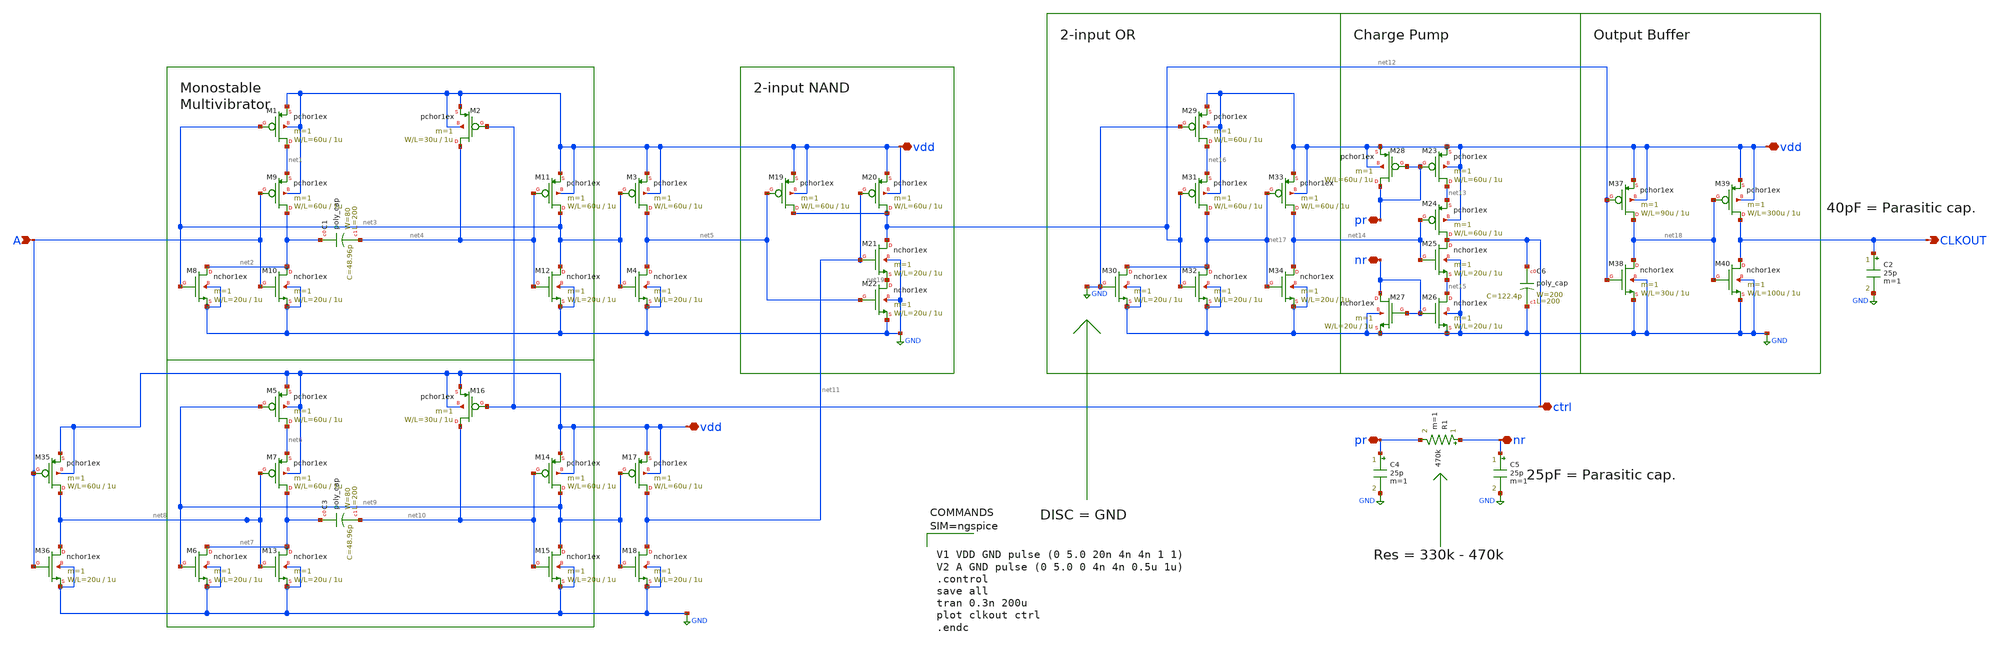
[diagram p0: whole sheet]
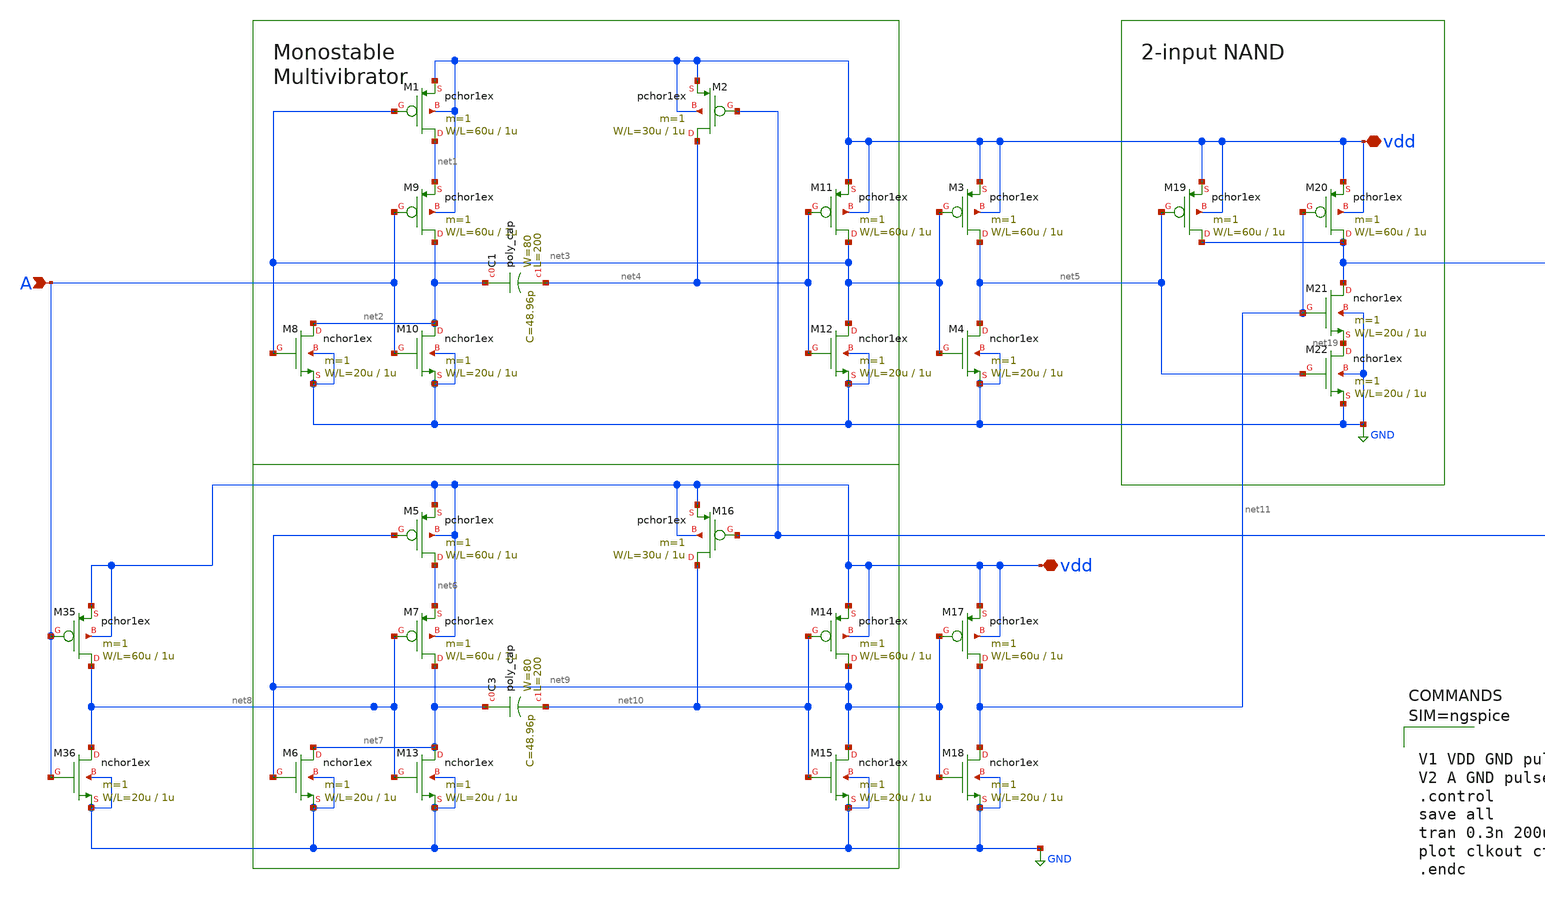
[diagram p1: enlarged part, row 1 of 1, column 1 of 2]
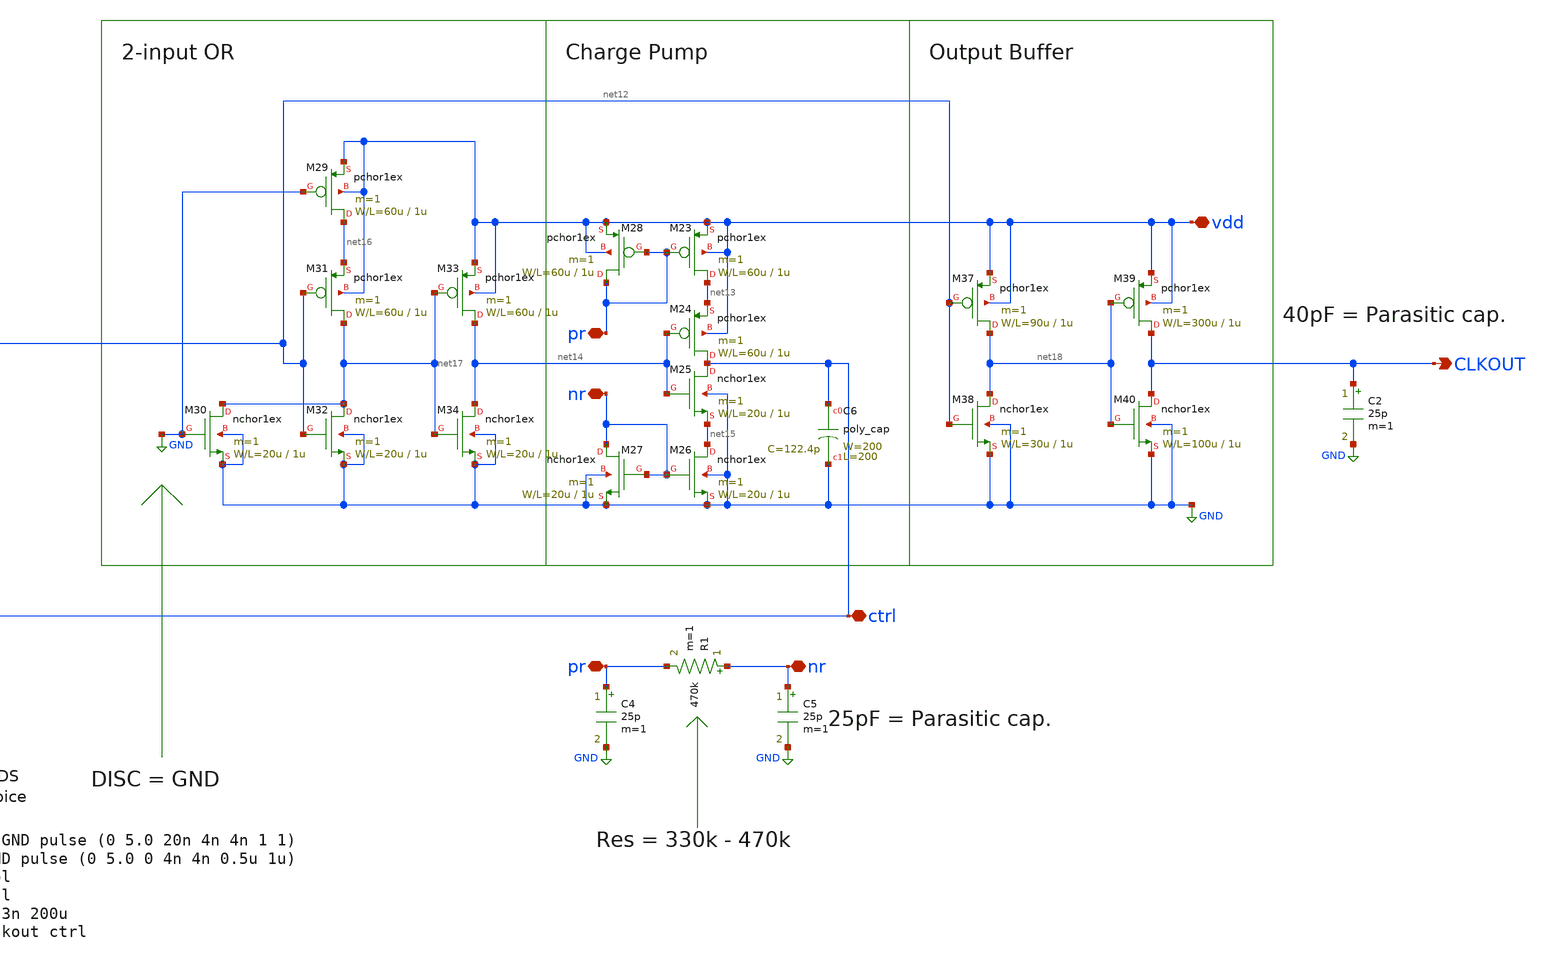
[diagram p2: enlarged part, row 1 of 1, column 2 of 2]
** sch_path: member_project/3zki/clkdb_testbench.sch
**.subckt clkdb_testbench ctrl pr nr CLKOUT vdd A vdd pr nr vdd
*.iopin ctrl
*.iopin pr
*.iopin nr
*.opin CLKOUT
*.iopin vdd
*.ipin A
*.iopin vdd
*.iopin pr
*.iopin nr
*.iopin vdd
C4 pr GND 25p m=1
C5 nr GND 25p m=1
R1 nr pr 470k m=1
C2 CLKOUT GND 25p m=1
M1 net1 net3 vdd vdd pchor1ex L=1u W=60u m=1
M8 net2 net3 GND GND nchor1ex L=1u W=20u m=1
M9 net2 A net1 vdd pchor1ex L=1u W=60u m=1
M10 net2 A GND GND nchor1ex L=1u W=20u m=1
M11 net3 net4 vdd vdd pchor1ex L=1u W=60u m=1
M12 net3 net4 GND GND nchor1ex L=1u W=20u m=1
C1 net2 net4 poly_cap W=80 L=200
M2 net4 ctrl vdd vdd pchor1ex L=1u W=30u m=1
M3 net5 net3 vdd vdd pchor1ex L=1u W=60u m=1
M4 net5 net3 GND GND nchor1ex L=1u W=20u m=1
M5 net6 net9 vdd vdd pchor1ex L=1u W=60u m=1
M6 net7 net9 GND GND nchor1ex L=1u W=20u m=1
M7 net7 net8 net6 vdd pchor1ex L=1u W=60u m=1
M13 net7 net8 GND GND nchor1ex L=1u W=20u m=1
M14 net9 net10 vdd vdd pchor1ex L=1u W=60u m=1
M15 net9 net10 GND GND nchor1ex L=1u W=20u m=1
C3 net7 net10 poly_cap W=80 L=200
M16 net10 ctrl vdd vdd pchor1ex L=1u W=30u m=1
M17 net11 net9 vdd vdd pchor1ex L=1u W=60u m=1
M18 net11 net9 GND GND nchor1ex L=1u W=20u m=1
M35 net8 A vdd vdd pchor1ex L=1u W=60u m=1
M36 net8 A GND GND nchor1ex L=1u W=20u m=1
M19 net12 net5 vdd vdd pchor1ex L=1u W=60u m=1
M20 net12 net11 vdd vdd pchor1ex L=1u W=60u m=1
M21 net12 net11 net19 GND nchor1ex L=1u W=20u m=1
M22 net19 net5 GND GND nchor1ex L=1u W=20u m=1
M23 net13 pr vdd vdd pchor1ex L=1u W=60u m=1
M24 ctrl net14 net13 vdd pchor1ex L=1u W=60u m=1
M25 ctrl net14 net15 GND nchor1ex L=1u W=20u m=1
M26 net15 nr GND GND nchor1ex L=1u W=20u m=1
M27 nr nr GND GND nchor1ex L=1u W=20u m=1
M28 pr pr vdd vdd pchor1ex L=1u W=60u m=1
C6 ctrl GND poly_cap W=200 L=200
M29 net16 GND vdd vdd pchor1ex L=1u W=60u m=1
M30 net17 GND GND GND nchor1ex L=1u W=20u m=1
M31 net17 net12 net16 vdd pchor1ex L=1u W=60u m=1
M32 net17 net12 GND GND nchor1ex L=1u W=20u m=1
M33 net14 net17 vdd vdd pchor1ex L=1u W=60u m=1
M34 net14 net17 GND GND nchor1ex L=1u W=20u m=1
M37 net18 net12 vdd vdd pchor1ex L=1u W=90u m=1
M38 net18 net12 GND GND nchor1ex L=1u W=30u m=1
M39 CLKOUT net18 vdd vdd pchor1ex L=1u W=300u m=1
M40 CLKOUT net18 GND GND nchor1ex L=1u W=100u m=1
**** begin user architecture code
 .include $::LIB/mos.lib
.include $::LIB/passive.lib
.include $::LIB/diode.lib



V1 VDD GND pulse (0 5.0 20n 4n 4n 1 1)
V2 A GND pulse (0 5.0 0 4n 4n 0.5u 1u)
.control
save all
tran 0.3n 200u
plot clkout ctrl
.endc



**** end user architecture code
**.ends
.GLOBAL GND
.end
